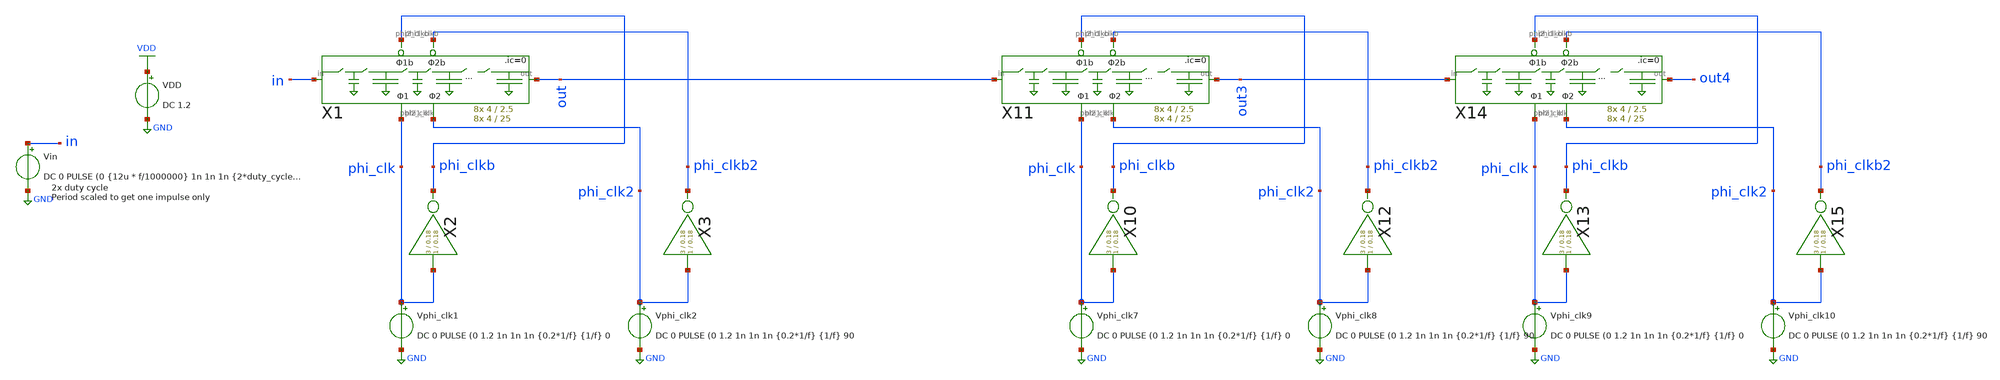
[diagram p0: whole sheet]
** sch_path: xschem/Switched_Caps/Multi_switchcaps_tb_scaled_impulse_2phi.sch
**.subckt Multi_switchcaps_tb_scaled_impulse_2phi
Vin in GND DC 0 PULSE (0 {12u * f/1000000} 1n 1n 1n {2*duty_cycle*1/f} {tend}
VDD VDD GND DC 1.2
X2 phi_clk phi_clkb inv Wpmos=3 Lpmos=0.18 Wnmos=1 Lnmos=0.18
Vphi_clk1 phi_clk GND DC 0 PULSE (0 1.2 1n 1n 1n {0.2*1/f} {1/f} 0
X1 in out phi_clk phi_clkb phi_clk2 phi_clkb2 16switchcaps_2phi Wcap1=4 Lcap1=2.5 Wcap2=4 Lcap2=25
Vphi_clk2 phi_clk2 GND DC 0 PULSE (0 1.2 1n 1n 1n {0.2*1/f} {1/f} 90
X3 phi_clk2 phi_clkb2 inv Wpmos=3 Lpmos=0.18 Wnmos=1 Lnmos=0.18
X10 phi_clk phi_clkb inv Wpmos=3 Lpmos=0.18 Wnmos=1 Lnmos=0.18
Vphi_clk7 phi_clk GND DC 0 PULSE (0 1.2 1n 1n 1n {0.2*1/f} {1/f} 0
X11 out out3 phi_clk phi_clkb phi_clk2 phi_clkb2 16switchcaps_2phi Wcap1=4 Lcap1=2.5 Wcap2=4
+ Lcap2=25
Vphi_clk8 phi_clk2 GND DC 0 PULSE (0 1.2 1n 1n 1n {0.2*1/f} {1/f} 90
X12 phi_clk2 phi_clkb2 inv Wpmos=3 Lpmos=0.18 Wnmos=1 Lnmos=0.18
X13 phi_clk phi_clkb inv Wpmos=3 Lpmos=0.18 Wnmos=1 Lnmos=0.18
Vphi_clk9 phi_clk GND DC 0 PULSE (0 1.2 1n 1n 1n {0.2*1/f} {1/f} 0
X14 out3 out4 phi_clk phi_clkb phi_clk2 phi_clkb2 16switchcaps_2phi Wcap1=4 Lcap1=2.5 Wcap2=4
+ Lcap2=25
Vphi_clk10 phi_clk2 GND DC 0 PULSE (0 1.2 1n 1n 1n {0.2*1/f} {1/f} 90
X15 phi_clk2 phi_clkb2 inv Wpmos=3 Lpmos=0.18 Wnmos=1 Lnmos=0.18
**** begin user architecture code


.lib /home/sky/sky130A/libs.tech/ngspice/sky130.lib.spice tt
.options abstol=1e-14 reltol=1e-4
.param f=2560k
.param duty_cycle=0.5
.param tau={(16^2)*1/f}
.param tend={4*tau}

*start all caps with 0 charge
.ic v(x1.x1.c1)=0 v(x1.c2)=0 v(x1.x2.c1)=0 v(x1.c4)=0   v(x1.x3.c1)=0 v(x1.c6)=0 v(x1.x4.c1)=0
+ v(x1.c8)=0   v(x1.x5.c1)=0 v(x1.c10)=0 v(x1.x6.c1)=0 v(x1.c12)=0   v(x1.x7.c1)=0 v(x1.c14)=0 v(x1.x8.c1)=0
+ v(out)=0  v(x11.x1.c1)=0 v(x11.c2)=0 v(x11.x2.c1)=0 v(x11.c4)=0   v(x11.x3.c1)=0 v(x11.c6)=0 v(x11.x4.c1)=0
+ v(x11.c8)=0   v(x11.x5.c1)=0 v(x11.c10)=0 v(x11.x6.c1)=0 v(x11.c12)=0   v(x11.x7.c1)=0 v(x11.c14)=0
+ v(x11.x8.c1)=0 v(out3)=0  v(x14.x1.c1)=0 v(x14.c2)=0 v(x14.x2.c1)=0 v(x14.c4)=0   v(x14.x3.c1)=0 v(x14.c6)=0
+ v(x14.x4.c1)=0 v(x14.c8)=0   v(x14.x5.c1)=0 v(x14.c10)=0 v(x14.x6.c1)=0 v(x14.c12)=0   v(x14.x7.c1)=0 v(x14.c14)=0
+ v(x14.x8.c1)=0 v(out4)=0

*.ac DEC 100 10 20k *doesn't seem to work, get 0s out
.tran {1/f} {tend}
.save all


**** end user architecture code
**.ends
.GLOBAL GND
.GLOBAL VDD
.end
